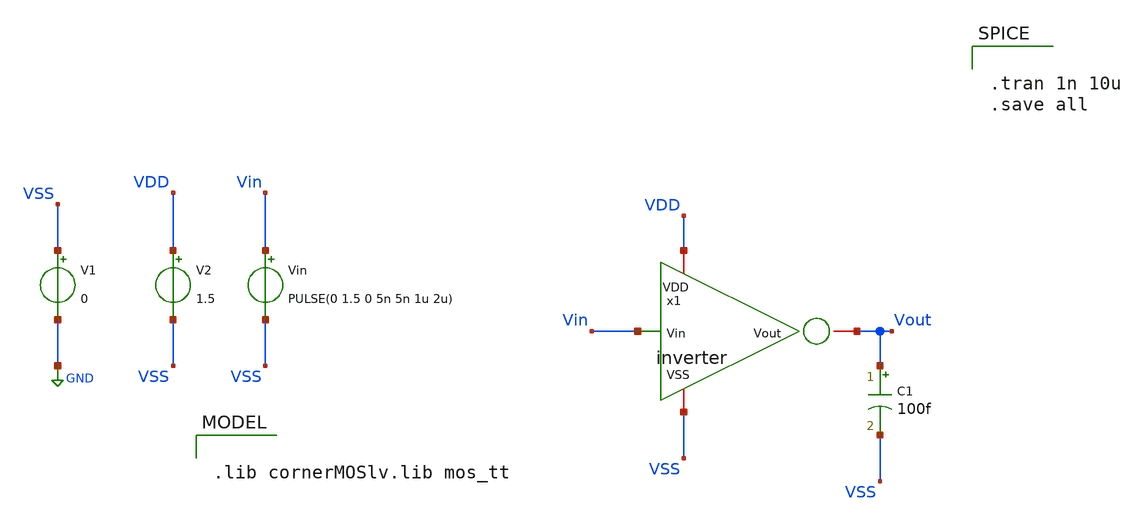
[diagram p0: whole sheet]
** sch_path: Modulo_Analogico/Lab5/inverter/xschem/inverter_tb_tran.sch
**.subckt inverter_tb_tran
x1 Vin VDD VSS Vout inverter
C1 Vout VSS 100f m=1
V1 VSS GND 0
V2 VDD VSS 1.5
Vin Vin VSS PULSE(0 1.5 0 5n 5n 1u 2u)
**** begin user architecture code


.tran 1n 10u
.save all



.lib cornerMOSlv.lib mos_tt

**** end user architecture code
**.ends
.GLOBAL GND
.end
